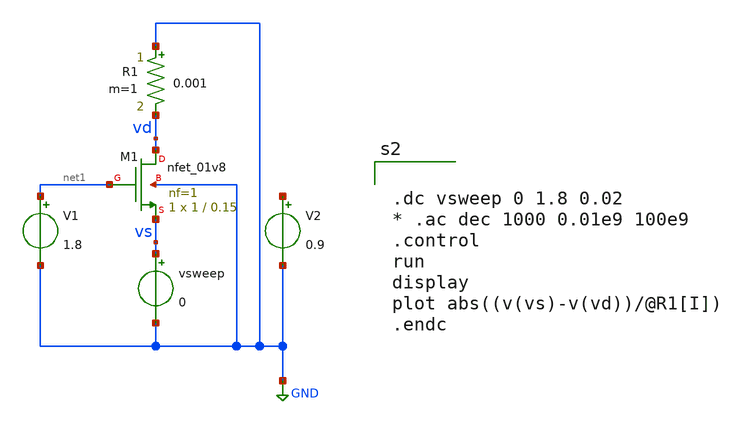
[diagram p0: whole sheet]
** sch_path: xschem/nfet_impedance_test.sch
**.subckt nfet_impedance_test
XM1 vd net1 vs GND sky130_fd_pr__nfet_01v8 L=0.15 W=1 nf=1 ad='int((nf+1)/2) * W/nf * 0.29' as='int((nf+2)/2) * W/nf * 0.29'
+ pd='2*int((nf+1)/2) * (W/nf + 0.29)' ps='2*int((nf+2)/2) * (W/nf + 0.29)' nrd='0.29 / W' nrs='0.29 / W'
+ sa=0 sb=0 sd=0 mult=1 m=1
V1 net1 GND 1.8
V2 net2 GND 0.9
R1 GND vd 0.001 m=1
vsweep vs GND 0
**** begin user architecture code
.lib $::SKYWATER_MODELS/sky130.lib.spice tt
* .include $::PDKPATH/libs.ref/sky130_fd_sc_hvl/spice/sky130_fd_sc_hvl.spice



.dc vsweep 0 1.8 0.02
* .ac dec 1000 0.01e9 100e9
.control
run
display
plot abs((v(vs)-v(vd))/@R1[I])
.endc


**** end user architecture code
**.ends
.GLOBAL GND
.end
